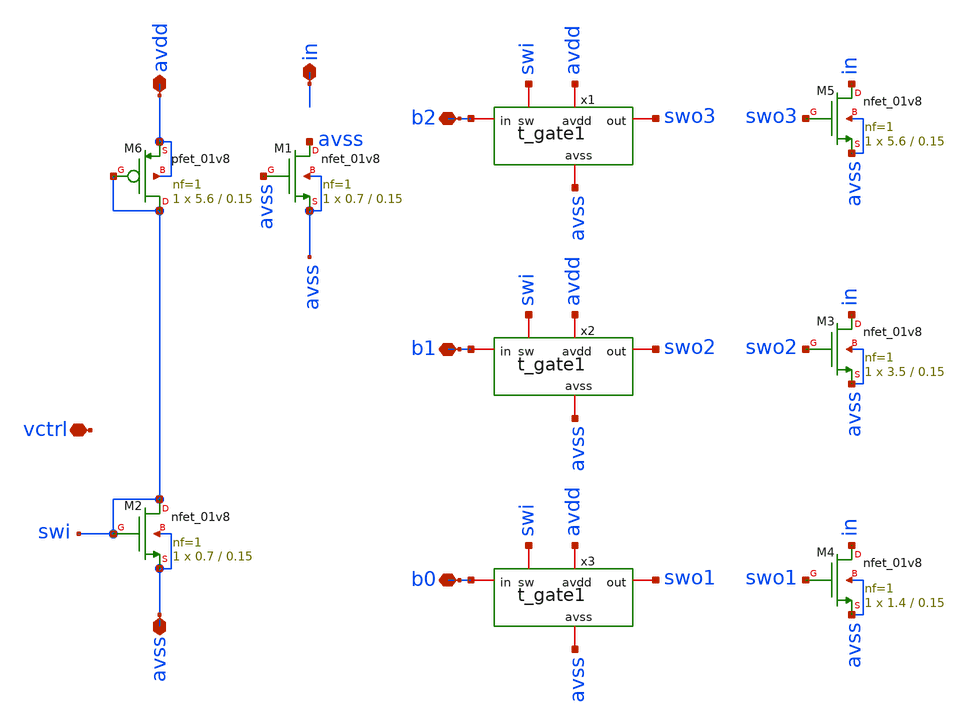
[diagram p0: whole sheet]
** sch_path: current_sw1.sch
**.subckt current_sw1 in avdd avss b0 b1 b2 vctrl
*.iopin in
*.iopin avdd
*.iopin avss
*.iopin b0
*.iopin b1
*.iopin b2
*.iopin vctrl
XM1 avss avss avss avss sky130_fd_pr__nfet_01v8 L=0.15 W=0.7 nf=1 ad='int((nf+1)/2) * W/nf * 0.29' as='int((nf+2)/2) * W/nf * 0.29'
+ pd='2*int((nf+1)/2) * (W/nf + 0.29)' ps='2*int((nf+2)/2) * (W/nf + 0.29)' nrd='0.29 / W' nrs='0.29 / W'
+ sa=0 sb=0 sd=0 mult=1 m=1
XM5 in swo3 avss avss sky130_fd_pr__nfet_01v8 L=0.15 W=5.6 nf=1 ad='int((nf+1)/2) * W/nf * 0.29' as='int((nf+2)/2) * W/nf * 0.29'
+ pd='2*int((nf+1)/2) * (W/nf + 0.29)' ps='2*int((nf+2)/2) * (W/nf + 0.29)' nrd='0.29 / W' nrs='0.29 / W'
+ sa=0 sb=0 sd=0 mult=1 m=1
XM3 in swo2 avss avss sky130_fd_pr__nfet_01v8 L=0.15 W=3.5 nf=1 ad='int((nf+1)/2) * W/nf * 0.29' as='int((nf+2)/2) * W/nf * 0.29'
+ pd='2*int((nf+1)/2) * (W/nf + 0.29)' ps='2*int((nf+2)/2) * (W/nf + 0.29)' nrd='0.29 / W' nrs='0.29 / W'
+ sa=0 sb=0 sd=0 mult=1 m=1
XM4 in swo1 avss avss sky130_fd_pr__nfet_01v8 L=0.15 W=1.4 nf=1 ad='int((nf+1)/2) * W/nf * 0.29' as='int((nf+2)/2) * W/nf * 0.29'
+ pd='2*int((nf+1)/2) * (W/nf + 0.29)' ps='2*int((nf+2)/2) * (W/nf + 0.29)' nrd='0.29 / W' nrs='0.29 / W'
+ sa=0 sb=0 sd=0 mult=1 m=1
XM2 swi swi avss avss sky130_fd_pr__nfet_01v8 L=0.15 W=0.7 nf=1 ad='int((nf+1)/2) * W/nf * 0.29' as='int((nf+2)/2) * W/nf * 0.29'
+ pd='2*int((nf+1)/2) * (W/nf + 0.29)' ps='2*int((nf+2)/2) * (W/nf + 0.29)' nrd='0.29 / W' nrs='0.29 / W'
+ sa=0 sb=0 sd=0 mult=1 m=1
XM6 swi swi avdd avdd sky130_fd_pr__pfet_01v8 L=0.15 W=5.6 nf=1 ad='int((nf+1)/2) * W/nf * 0.29' as='int((nf+2)/2) * W/nf * 0.29'
+ pd='2*int((nf+1)/2) * (W/nf + 0.29)' ps='2*int((nf+2)/2) * (W/nf + 0.29)' nrd='0.29 / W' nrs='0.29 / W'
+ sa=0 sb=0 sd=0 mult=1 m=1
x1 swo3 b2 avss avdd swi t_gate1
x2 swo2 b1 avss avdd swi t_gate1
x3 swo1 b0 avss avdd swi t_gate1
**.ends

* expanding   symbol:  ma2022/t_gate1.sym # of pins=5
** sym_path: xschem/t_gate1.sym
** sch_path: xschem/t_gate1.sch
.subckt t_gate1 out in avss avdd sw
*.iopin in
*.iopin avdd
*.iopin avss
*.iopin sw
*.iopin out
XM17 out sw in avdd sky130_fd_pr__pfet_01v8 L=0.15 W=1.4 nf=1 ad='int((nf+1)/2) * W/nf * 0.29' as='int((nf+2)/2) * W/nf * 0.29'
+ pd='2*int((nf+1)/2) * (W/nf + 0.29)' ps='2*int((nf+2)/2) * (W/nf + 0.29)' nrd='0.29 / W' nrs='0.29 / W'
+ sa=0 sb=0 sd=0 mult=1 m=1
XM18 in net1 out avss sky130_fd_pr__nfet_01v8 L=0.15 W=1.4 nf=1 ad='int((nf+1)/2) * W/nf * 0.29' as='int((nf+2)/2) * W/nf * 0.29'
+ pd='2*int((nf+1)/2) * (W/nf + 0.29)' ps='2*int((nf+2)/2) * (W/nf + 0.29)' nrd='0.29 / W' nrs='0.29 / W'
+ sa=0 sb=0 sd=0 mult=1 m=1
x1 avdd sw net1 avss inv_simple1
.ends


* expanding   symbol:  ma2022/inv_simple1.sym # of pins=4
** sym_path: xschem/inv_simple1.sym
** sch_path: xschem/inv_simple1.sch
.subckt inv_simple1 vdd in out vss
*.iopin in
*.iopin vdd
*.iopin vss
*.iopin out
XM19 out in vss vss sky130_fd_pr__nfet_01v8 L=0.15 W=1.4 nf=1 ad='int((nf+1)/2) * W/nf * 0.29' as='int((nf+2)/2) * W/nf * 0.29'
+ pd='2*int((nf+1)/2) * (W/nf + 0.29)' ps='2*int((nf+2)/2) * (W/nf + 0.29)' nrd='0.29 / W' nrs='0.29 / W'
+ sa=0 sb=0 sd=0 mult=1 m=1
XM20 out in vdd vdd sky130_fd_pr__pfet_01v8 L=0.15 W=2.8 nf=1 ad='int((nf+1)/2) * W/nf * 0.29' as='int((nf+2)/2) * W/nf * 0.29'
+ pd='2*int((nf+1)/2) * (W/nf + 0.29)' ps='2*int((nf+2)/2) * (W/nf + 0.29)' nrd='0.29 / W' nrs='0.29 / W'
+ sa=0 sb=0 sd=0 mult=1 m=1
XM1 vdd vdd vdd vdd sky130_fd_pr__pfet_01v8 L=0.15 W=1.4 nf=1 ad='int((nf+1)/2) * W/nf * 0.29' as='int((nf+2)/2) * W/nf * 0.29'
+ pd='2*int((nf+1)/2) * (W/nf + 0.29)' ps='2*int((nf+2)/2) * (W/nf + 0.29)' nrd='0.29 / W' nrs='0.29 / W'
+ sa=0 sb=0 sd=0 mult=1 m=1
XM2 vss vss vss vss sky130_fd_pr__nfet_01v8 L=0.15 W=1.4 nf=1 ad='int((nf+1)/2) * W/nf * 0.29' as='int((nf+2)/2) * W/nf * 0.29'
+ pd='2*int((nf+1)/2) * (W/nf + 0.29)' ps='2*int((nf+2)/2) * (W/nf + 0.29)' nrd='0.29 / W' nrs='0.29 / W'
+ sa=0 sb=0 sd=0 mult=1 m=1
.ends

.end
